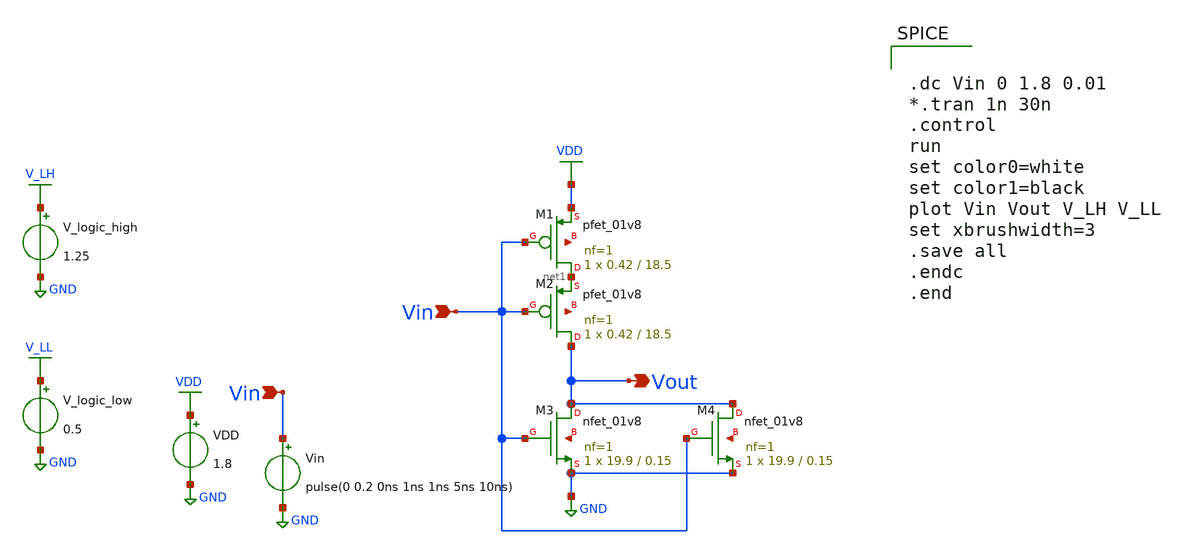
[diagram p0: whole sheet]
** sch_path: xschem/Vth_sch/Inverter-th4.sch
**.subckt Inverter-th4 Vin Vin Vout
*.ipin Vin
*.ipin Vin
*.opin Vout
VDD VDD GND 1.8
Vin Vin GND pulse(0 0.2 0ns 1ns 1ns 5ns 10ns)
XM1 net1 Vin VDD net2 sky130_fd_pr__pfet_01v8 L=18.5 W=0.42 nf=1 ad='int((nf+1)/2) * W/nf * 0.29' as='int((nf+2)/2) * W/nf * 0.29'
+ pd='2*int((nf+1)/2) * (W/nf + 0.29)' ps='2*int((nf+2)/2) * (W/nf + 0.29)' nrd='0.29 / W' nrs='0.29 / W'
+ sa=0 sb=0 sd=0 mult=1 m=1
V_logic_high V_LH GND 1.25
V_logic_low V_LL GND 0.5
XM3 Vout Vin GND net3 sky130_fd_pr__nfet_01v8 L=0.15 W=19.9 nf=1 ad='int((nf+1)/2) * W/nf * 0.29' as='int((nf+2)/2) * W/nf * 0.29'
+ pd='2*int((nf+1)/2) * (W/nf + 0.29)' ps='2*int((nf+2)/2) * (W/nf + 0.29)' nrd='0.29 / W' nrs='0.29 / W'
+ sa=0 sb=0 sd=0 mult=1 m=1
XM2 Vout Vin net1 net4 sky130_fd_pr__pfet_01v8 L=18.5 W=0.42 nf=1 ad='int((nf+1)/2) * W/nf * 0.29' as='int((nf+2)/2) * W/nf * 0.29'
+ pd='2*int((nf+1)/2) * (W/nf + 0.29)' ps='2*int((nf+2)/2) * (W/nf + 0.29)' nrd='0.29 / W' nrs='0.29 / W'
+ sa=0 sb=0 sd=0 mult=1 m=1
XM4 Vout Vin GND net5 sky130_fd_pr__nfet_01v8 L=0.15 W=19.9 nf=1 ad='int((nf+1)/2) * W/nf * 0.29' as='int((nf+2)/2) * W/nf * 0.29'
+ pd='2*int((nf+1)/2) * (W/nf + 0.29)' ps='2*int((nf+2)/2) * (W/nf + 0.29)' nrd='0.29 / W' nrs='0.29 / W'
+ sa=0 sb=0 sd=0 mult=1 m=1
**** begin user architecture code


.lib /usr/local/share/pdk/sky130A/libs.tech/ngspice/sky130.lib.spice tt

.save all





.dc Vin 0 1.8 0.01
*.tran 1n 30n
.control
run
set color0=white
set color1=black
plot Vin Vout V_LH V_LL
set xbrushwidth=3
.save all
.endc
.end


**** end user architecture code
**.ends
.GLOBAL VDD
.GLOBAL GND
.GLOBAL V_LH
.GLOBAL V_LL
.end
